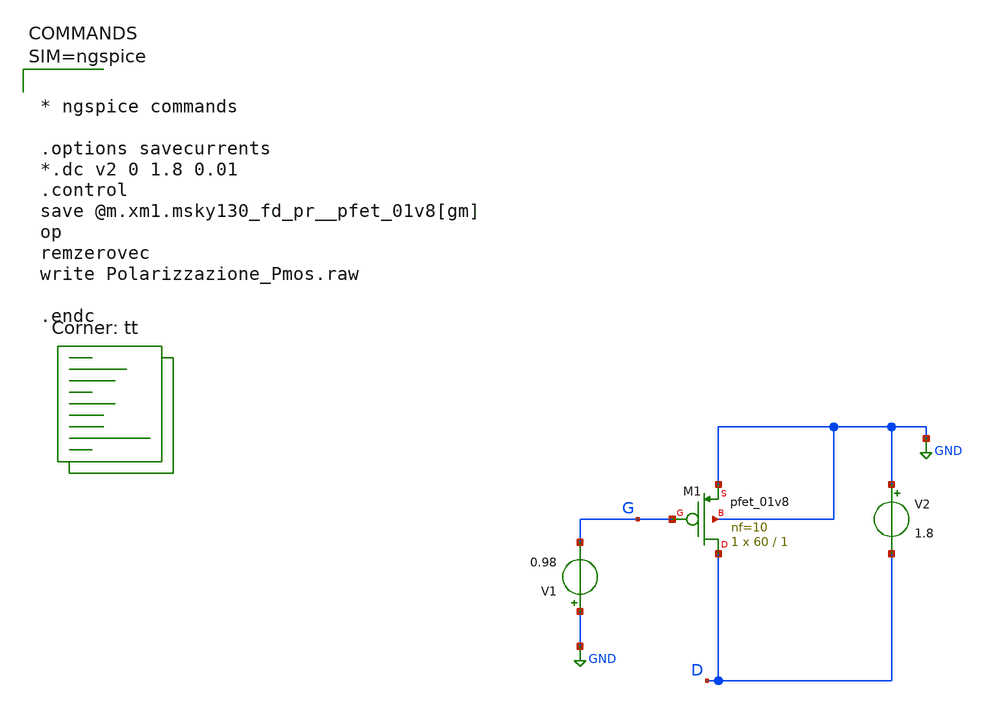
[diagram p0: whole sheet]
** sch_path: xschem/Polarizzazione_Pmos.sch
* Copyright 2021 Stefan Frederik Schippers
* Licensed under the Apache License, Version 2.0 (the "License");
* you may not use this file except in compliance with the License.
* You may obtain a copy of the License at
* https://www.apache.org/licenses/LICENSE-2.0
* Unless required by applicable law or agreed to in writing, software
* distributed under the License is distributed on an "AS IS" BASIS,
* WITHOUT WARRANTIES OR CONDITIONS OF ANY KIND, either express or implied.
* See the License for the specific language governing permissions and
* limitations under the License.
**.subckt Polarizzazione_Pmos
V1 GND G 0.98
V2 GND D 1.8
XM1 D G GND GND sky130_fd_pr__pfet_01v8 L=1 W=60 nf=10 ad='int((nf+1)/2) * W/nf * 0.29' as='int((nf+2)/2) * W/nf * 0.29'
+ pd='2*int((nf+1)/2) * (W/nf + 0.29)' ps='2*int((nf+2)/2) * (W/nf + 0.29)' nrd='0.29 / W' nrs='0.29 / W'
+ sa=0 sb=0 sd=0 mult=1 m=1
**** begin user architecture code



* ngspice commands

.options savecurrents
*.dc v2 0 1.8 0.01
.control
save @m.xm1.msky130_fd_pr__pfet_01v8[gm]
op
remzerovec
write Polarizzazione_Pmos.raw

.endc



.lib $::SKYWATER_MODELS/sky130.lib.spice tt
**** end user architecture code
**.ends
.GLOBAL GND
.end
